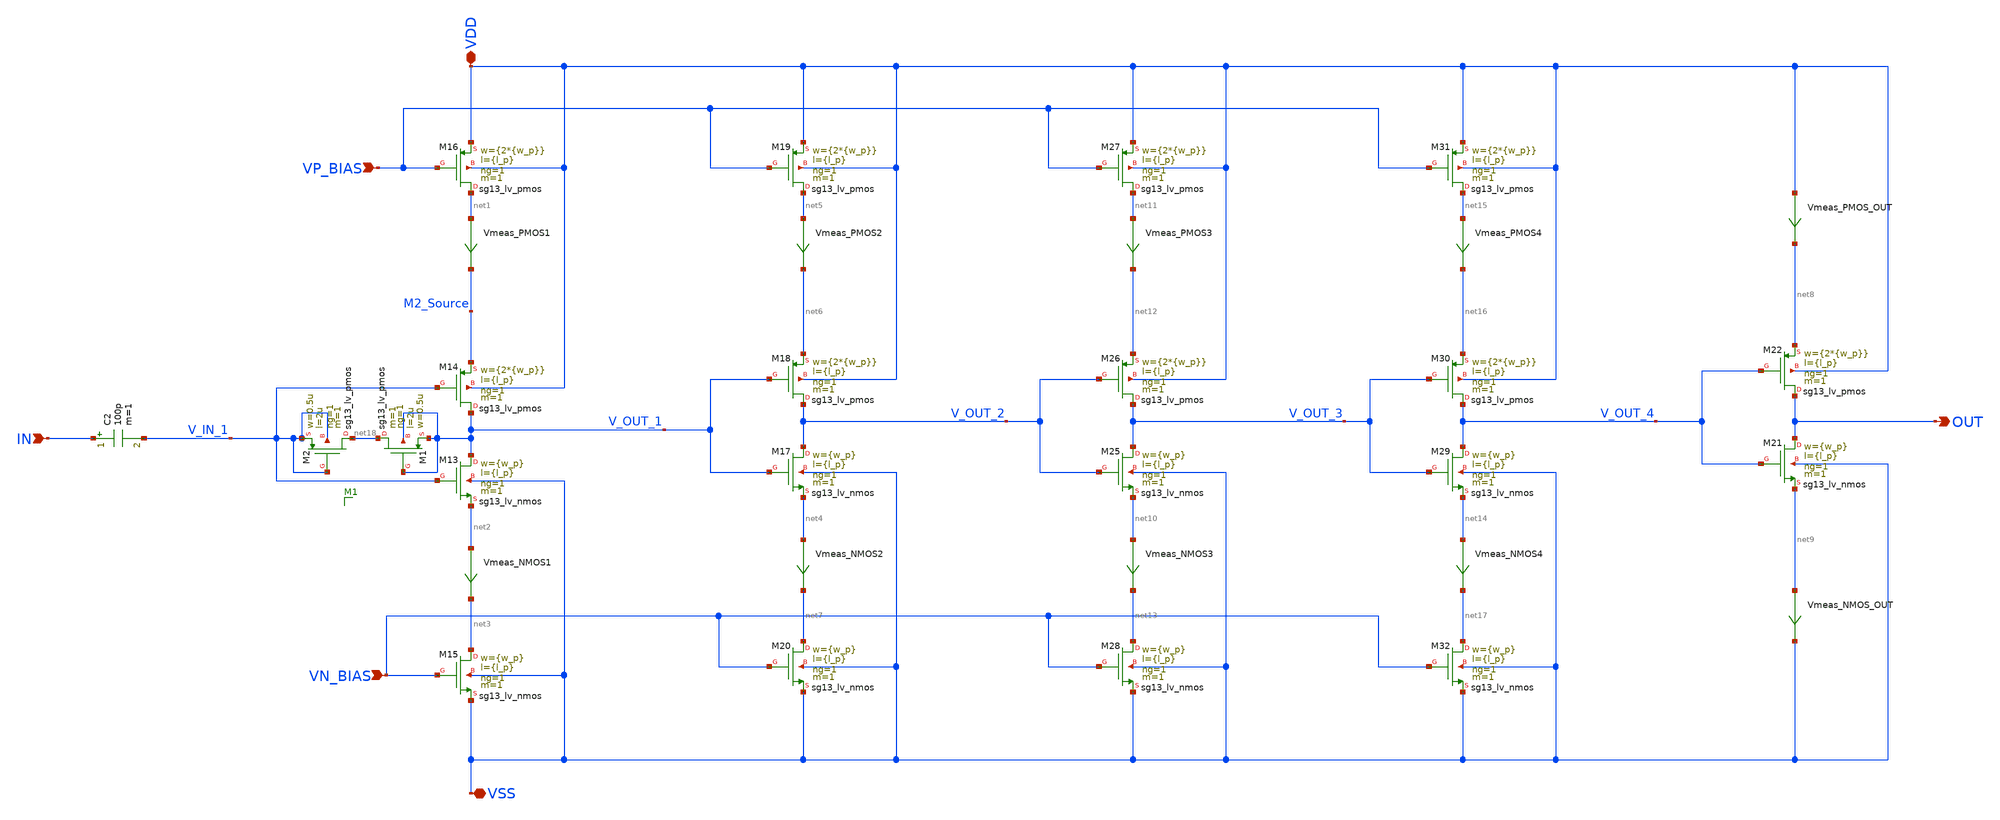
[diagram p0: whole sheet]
** sch_path: clock_gen.sch
**.subckt clock_gen IN VSS OUT VDD VP_BIAS VN_BIAS
*.ipin IN
*.iopin VSS
*.opin OUT
*.iopin VDD
*.ipin VP_BIAS
*.ipin VN_BIAS
XM13 V_OUT_1 V_IN_1 net2 VSS sg13_lv_nmos w={w_p} l={l_p} ng=1 m=1 mm_ok=1
XM14 V_OUT_1 V_IN_1 M2_Source VDD sg13_lv_pmos w={2*{w_p}} l={l_p} ng=1 m=1 mm_ok=1
XM15 net3 VN_BIAS VSS VSS sg13_lv_nmos w={w_p} l={l_p} ng=1 m=1 mm_ok=1
XM16 net1 VP_BIAS VDD VDD sg13_lv_pmos w={2*{w_p}} l={l_p} ng=1 m=1 mm_ok=1
Vmeas_PMOS1 net1 M2_Source 0
.save i(vmeas_pmos1)
Vmeas_NMOS1 net2 net3 0
.save i(vmeas_nmos1)
C2 IN V_IN_1 100p m=1
XM17 V_OUT_2 V_OUT_1 net4 VSS sg13_lv_nmos w={w_p} l={l_p} ng=1 m=1 mm_ok=1
XM18 V_OUT_2 V_OUT_1 net6 VDD sg13_lv_pmos w={2*{w_p}} l={l_p} ng=1 m=1 mm_ok=1
Vmeas_NMOS2 net4 net7 0
.save i(vmeas_nmos2)
XM19 net5 VP_BIAS VDD VDD sg13_lv_pmos w={2*{w_p}} l={l_p} ng=1 m=1 mm_ok=1
Vmeas_PMOS2 net5 net6 0
.save i(vmeas_pmos2)
XM20 net7 VN_BIAS VSS VSS sg13_lv_nmos w={w_p} l={l_p} ng=1 m=1 mm_ok=1
XM21 OUT V_OUT_4 net9 VSS sg13_lv_nmos w={w_p} l={l_p} ng=1 m=1 mm_ok=1
XM22 OUT V_OUT_4 net8 VDD sg13_lv_pmos w={2*{w_p}} l={l_p} ng=1 m=1 mm_ok=1
Vmeas_PMOS_OUT VDD net8 0
.save i(vmeas_pmos_out)
Vmeas_NMOS_OUT net9 VSS 0
.save i(vmeas_nmos_out)
XM25 V_OUT_3 V_OUT_2 net10 VSS sg13_lv_nmos w={w_p} l={l_p} ng=1 m=1 mm_ok=1
XM26 V_OUT_3 V_OUT_2 net12 VDD sg13_lv_pmos w={2*{w_p}} l={l_p} ng=1 m=1 mm_ok=1
Vmeas_NMOS3 net10 net13 0
.save i(vmeas_nmos3)
XM27 net11 VP_BIAS VDD VDD sg13_lv_pmos w={2*{w_p}} l={l_p} ng=1 m=1 mm_ok=1
Vmeas_PMOS3 net11 net12 0
.save i(vmeas_pmos3)
XM28 net13 VN_BIAS VSS VSS sg13_lv_nmos w={w_p} l={l_p} ng=1 m=1 mm_ok=1
XM29 V_OUT_4 V_OUT_3 net14 VSS sg13_lv_nmos w={w_p} l={l_p} ng=1 m=1 mm_ok=1
XM30 V_OUT_4 V_OUT_3 net16 VDD sg13_lv_pmos w={2*{w_p}} l={l_p} ng=1 m=1 mm_ok=1
Vmeas_NMOS4 net14 net17 0
.save i(vmeas_nmos4)
XM31 net15 VP_BIAS VDD VDD sg13_lv_pmos w={2*{w_p}} l={l_p} ng=1 m=1 mm_ok=1
Vmeas_PMOS4 net15 net16 0
.save i(vmeas_pmos4)
XM32 net17 VN_BIAS VSS VSS sg13_lv_nmos w={w_p} l={l_p} ng=1 m=1 mm_ok=1
XM1 net18 V_OUT_1 V_OUT_1 V_OUT_1 sg13_lv_pmos w=0.5u l=2u ng=1 m=1 mm_ok=1
XM2 net18 V_IN_1 V_IN_1 V_IN_1 sg13_lv_pmos w=0.5u l=2u ng=1 m=1 mm_ok=1
**.ends
.end
